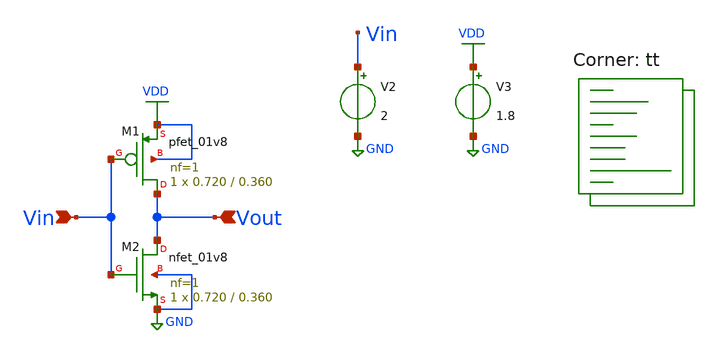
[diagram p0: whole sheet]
** sch_path: xschem/inverter/inverter_operatingPoint.sch
**.subckt inverter_operatingPoint Vin Vout
*.ipin Vin
*.ipin Vout
V2 Vin GND 2
V3 VDD GND 1.8
XM1 Vout Vin VDD VDD sky130_fd_pr__pfet_01v8 L=0.360 W=0.720 nf=1 ad='int((nf+1)/2) * W/nf * 0.29' as='int((nf+2)/2) * W/nf * 0.29'
+ pd='2*int((nf+1)/2) * (W/nf + 0.29)' ps='2*int((nf+2)/2) * (W/nf + 0.29)' nrd='0.29 / W' nrs='0.29 / W'
+ sa=0 sb=0 sd=0 mult=1 m=1
XM2 Vout Vin GND GND sky130_fd_pr__nfet_01v8 L=0.360 W=0.720 nf=1 ad='int((nf+1)/2) * W/nf * 0.29' as='int((nf+2)/2) * W/nf * 0.29'
+ pd='2*int((nf+1)/2) * (W/nf + 0.29)' ps='2*int((nf+2)/2) * (W/nf + 0.29)' nrd='0.29 / W' nrs='0.29 / W'
+ sa=0 sb=0 sd=0 mult=1 m=1
**** begin user architecture code
.lib $::SKYWATER_MODELS/sky130.lib.spice tt
**** end user architecture code
**.ends
.GLOBAL GND
.GLOBAL VDD
**** begin user architecture code

.options savecurrents
.control
save @m.xm2.msky130_fd_pr__nfet_01v8[gm]
save @m.xm2.msky130_fd_pr__nfet_01v8[vgs]
save @m.xm2.msky130_fd_pr__nfet_01v8[vds]
save @m.xm2.msky130_fd_pr__nfet_01v8[vth]
save @m.xm2.msky130_fd_pr__nfet_01v8[ids]
save @m.xm1.msky130_fd_pr__pfet_01v8[gm]
save @m.xm1.msky130_fd_pr__pfet_01v8[vgs]
save @m.xm1.msky130_fd_pr__pfet_01v8[vds]
save @m.xm1.msky130_fd_pr__pfet_01v8[vth]
save @m.xm1.msky130_fd_pr__pfet_01v8[ids]
.save all
op
write inverter_operatingPoint.raw
.endc


**** end user architecture code
.end
